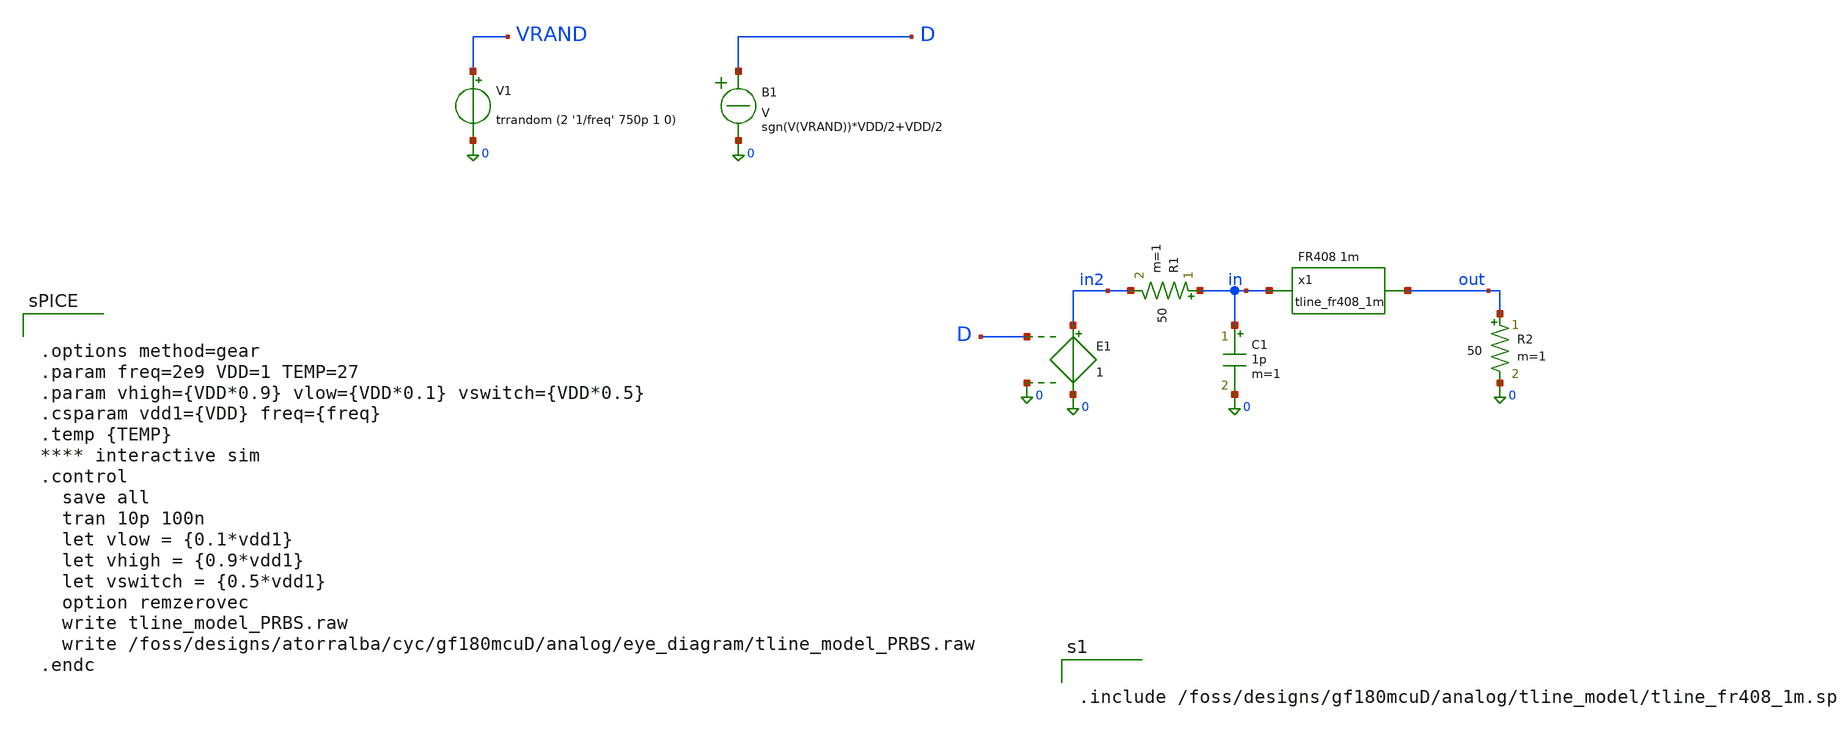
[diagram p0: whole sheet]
** sch_path: Python_tools/channel_model/tline_model_PRBS.sch
**.subckt tline_model_PRBS
V1 VRAND 0 trrandom (2 '1/freq' 750p 1 0)
B1 D 0 V = sgn(V(VRAND))*VDD/2+VDD/2
E1 in2 0 D 0 1
R1 in in2 50 m=1
R2 out 0 50 m=1
C1 in 0 1p m=1
x1 in out tline_fr408_1m
**** begin user architecture code


.options method=gear
.param freq=2e9 VDD=1 TEMP=27
.param vhigh={VDD*0.9} vlow={VDD*0.1} vswitch={VDD*0.5}
.csparam vdd1={VDD} freq={freq}
.temp {TEMP}
**** interactive sim
.control
  save all
  tran 10p 100n
  let vlow = {0.1*vdd1}
  let vhigh = {0.9*vdd1}
  let vswitch = {0.5*vdd1}
  option remzerovec
  write tline_model_PRBS.raw
  write /foss/designs/atorralba/cyc/gf180mcuD/analog/eye_diagram/tline_model_PRBS.raw
.endc




.include /foss/designs/gf180mcuD/analog/tline_model/tline_fr408_1m.sp

**** end user architecture code
**.ends
.end
